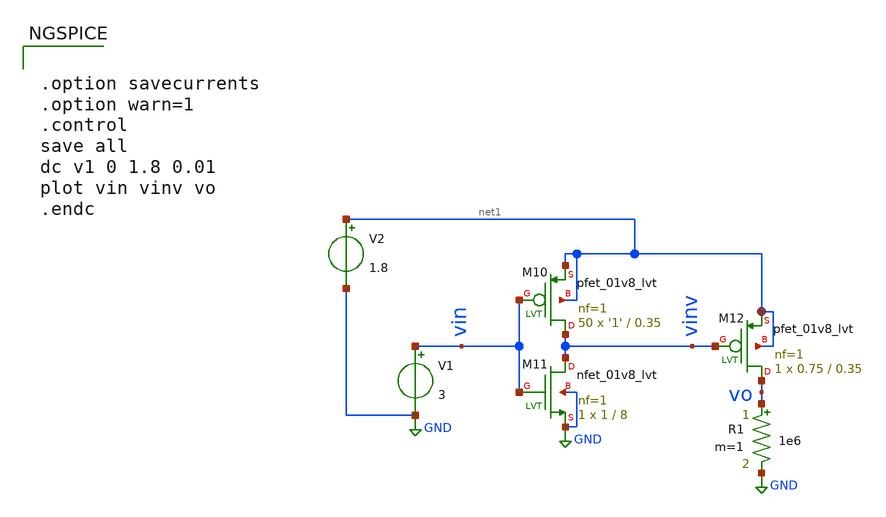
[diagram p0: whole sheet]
** sch_path: schematics/startup-ckt.sch
**.subckt startup-ckt
XM10 vinv vin net1 net1 sky130_fd_pr__pfet_01v8_lvt L=0.35 W='1' nf=1 ad='int((nf+1)/2) * W/nf * 0.29'
+ as='int((nf+2)/2) * W/nf * 0.29' pd='2*int((nf+1)/2) * (W/nf + 0.29)' ps='2*int((nf+2)/2) * (W/nf + 0.29)'
+ nrd='0.29 / W' nrs='0.29 / W' sa=0 sb=0 sd=0 mult=50 m=50
XM11 vinv vin GND GND sky130_fd_pr__nfet_01v8_lvt L=8 W=1 nf=1 ad='int((nf+1)/2) * W/nf * 0.29' as='int((nf+2)/2) * W/nf * 0.29'
+ pd='2*int((nf+1)/2) * (W/nf + 0.29)' ps='2*int((nf+2)/2) * (W/nf + 0.29)' nrd='0.29 / W' nrs='0.29 / W'
+ sa=0 sb=0 sd=0 mult=1 m=1
XM12 vo vinv net1 net1 sky130_fd_pr__pfet_01v8_lvt L=0.35 W=0.75 nf=1 ad='int((nf+1)/2) * W/nf * 0.29'
+ as='int((nf+2)/2) * W/nf * 0.29' pd='2*int((nf+1)/2) * (W/nf + 0.29)' ps='2*int((nf+2)/2) * (W/nf + 0.29)'
+ nrd='0.29 / W' nrs='0.29 / W' sa=0 sb=0 sd=0 mult=1 m=1
V1 vin GND 3
V2 net1 GND 1.8
R1 vo GND 1e6 m=1
**** begin user architecture code

.include $::SKYWATER_MODELS/cells/nfet_01v8/sky130_fd_pr__nfet_01v8__tt.corner.spice
.include $::SKYWATER_MODELS/cells/nfet_01v8_lvt/sky130_fd_pr__nfet_01v8_lvt__tt.corner.spice
.include $::SKYWATER_MODELS/cells/pfet_01v8/sky130_fd_pr__pfet_01v8__tt.corner.spice
.include $::SKYWATER_MODELS/cells/nfet_03v3_nvt/sky130_fd_pr__nfet_03v3_nvt__tt.corner.spice
.include $::SKYWATER_MODELS/cells/nfet_05v0_nvt/sky130_fd_pr__nfet_05v0_nvt__tt.corner.spice
.include $::SKYWATER_MODELS/cells/esd_nfet_01v8/sky130_fd_pr__esd_nfet_01v8__tt.corner.spice
.include $::SKYWATER_MODELS/cells/pfet_01v8_lvt/sky130_fd_pr__pfet_01v8_lvt__tt.corner.spice
.include $::SKYWATER_MODELS/cells/pfet_01v8_hvt/sky130_fd_pr__pfet_01v8_hvt__tt.corner.spice
.include $::SKYWATER_MODELS/cells/esd_pfet_g5v0d10v5/sky130_fd_pr__esd_pfet_g5v0d10v5__tt.corner.spice
.include $::SKYWATER_MODELS/cells/pfet_g5v0d10v5/sky130_fd_pr__pfet_g5v0d10v5__tt.corner.spice
.include $::SKYWATER_MODELS/cells/pfet_g5v0d16v0/sky130_fd_pr__pfet_g5v0d16v0__tt.corner.spice
.include $::SKYWATER_MODELS/cells/nfet_g5v0d10v5/sky130_fd_pr__nfet_g5v0d10v5__tt.corner.spice
.include $::SKYWATER_MODELS/cells/nfet_g5v0d16v0/sky130_fd_pr__nfet_g5v0d16v0__tt_discrete.corner.spice
.include $::SKYWATER_MODELS/cells/esd_nfet_g5v0d10v5/sky130_fd_pr__esd_nfet_g5v0d10v5__tt.corner.spice
.include $::SKYWATER_MODELS/models/corners/tt/nonfet.spice
* Mismatch parameters
.include $::SKYWATER_MODELS/cells/nfet_01v8/sky130_fd_pr__nfet_01v8__mismatch.corner.spice
.include $::SKYWATER_MODELS/cells/pfet_01v8/sky130_fd_pr__pfet_01v8__mismatch.corner.spice
.include $::SKYWATER_MODELS/cells/nfet_01v8_lvt/sky130_fd_pr__nfet_01v8_lvt__mismatch.corner.spice
.include $::SKYWATER_MODELS/cells/pfet_01v8_lvt/sky130_fd_pr__pfet_01v8_lvt__mismatch.corner.spice
.include $::SKYWATER_MODELS/cells/pfet_01v8_hvt/sky130_fd_pr__pfet_01v8_hvt__mismatch.corner.spice
.include $::SKYWATER_MODELS/cells/nfet_g5v0d10v5/sky130_fd_pr__nfet_g5v0d10v5__mismatch.corner.spice
.include $::SKYWATER_MODELS/cells/pfet_g5v0d10v5/sky130_fd_pr__pfet_g5v0d10v5__mismatch.corner.spice
.include $::SKYWATER_MODELS/cells/nfet_05v0_nvt/sky130_fd_pr__nfet_05v0_nvt__mismatch.corner.spice
.include $::SKYWATER_MODELS/cells/nfet_03v3_nvt/sky130_fd_pr__nfet_03v3_nvt__mismatch.corner.spice
* Resistor$::SKYWATER_MODELS/Capacitor
.include $::SKYWATER_MODELS/models/r+c/res_typical__cap_typical.spice
.include $::SKYWATER_MODELS/models/r+c/res_typical__cap_typical__lin.spice
* Special cells
.include $::SKYWATER_MODELS/models/corners/tt/specialized_cells.spice
* All models
.include $::SKYWATER_MODELS/models/all.spice
.include $::SKYWATER_MODELS/cells/pnp_05v5/sky130_fd_pr__pnp_05v5_W3p40L3p40.model.spice
* Corner
.include $::SKYWATER_MODELS/models/corners/tt/rf.spice



.option savecurrents
.option warn=1
.control
save all
dc v1 0 1.8 0.01
plot vin vinv vo
.endc


**** end user architecture code
**.ends
.GLOBAL GND
.end
